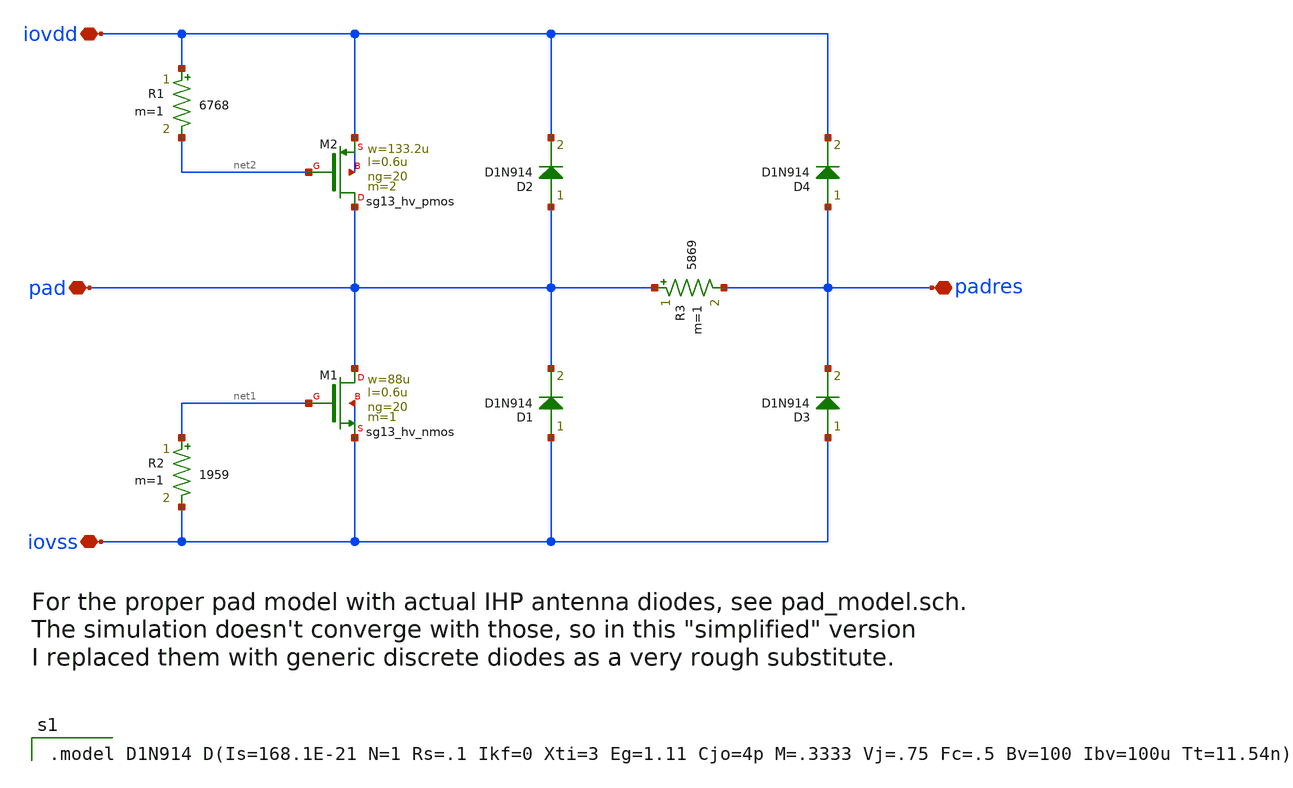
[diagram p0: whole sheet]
** sch_path: xschem/pad_model_simp2.sch
**.subckt pad_model_simp2 pad padres iovdd iovss
*.iopin pad
*.iopin padres
*.iopin iovdd
*.iopin iovss
XM2 pad net2 iovdd iovdd sg13_hv_pmos w=133.2u l=0.6u ng=20 m=2 mm_ok=1
XM1 pad net1 iovss iovss sg13_hv_nmos w=88u l=0.6u ng=20 m=1 mm_ok=1
D1 iovss pad D1N914 area=1
D2 pad iovdd D1N914 area=1
D3 iovss padres D1N914 area=1
D4 padres iovdd D1N914 area=1
R1 iovdd net2 6768 m=1
R2 net1 iovss 1959 m=1
R3 pad padres 5869 m=1
**** begin user architecture code

.model D1N914 D(Is=168.1E-21 N=1 Rs=.1 Ikf=0 Xti=3 Eg=1.11 Cjo=4p M=.3333 Vj=.75 Fc=.5 Bv=100
+ Ibv=100u Tt=11.54n)

**** end user architecture code
**.ends
.end
